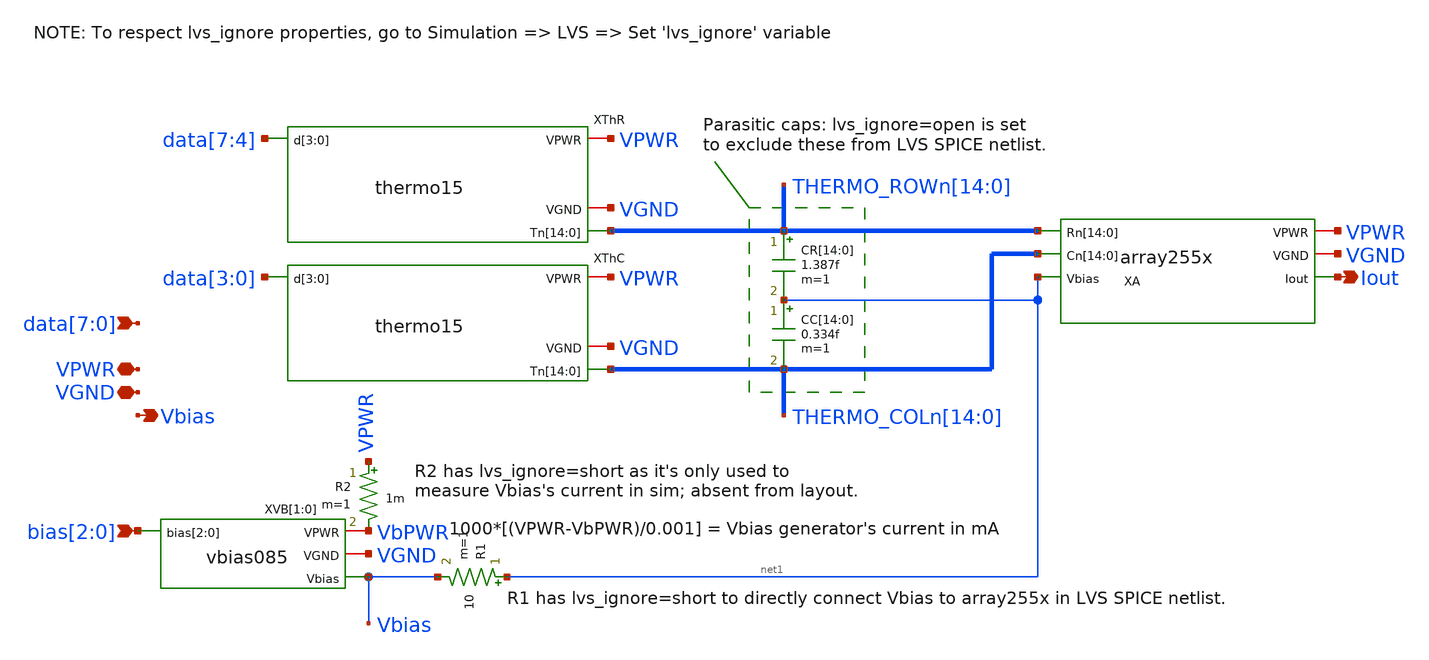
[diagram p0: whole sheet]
** sch_path: xschem/csdac255.sch
**.subckt csdac255 VPWR Iout VGND bias[2],bias[1],bias[0]
*+ data[7],data[6],data[5],data[4],data[3],data[2],data[1],data[0] Vbias
*.iopin VPWR
*.opin Iout
*.iopin VGND
*.ipin bias[2],bias[1],bias[0]
*.ipin data[7],data[6],data[5],data[4],data[3],data[2],data[1],data[0]
*.opin Vbias
XThR VPWR VGND THERMO_ROWn[14] THERMO_ROWn[13] THERMO_ROWn[12] THERMO_ROWn[11] THERMO_ROWn[10]
+ THERMO_ROWn[9] THERMO_ROWn[8] THERMO_ROWn[7] THERMO_ROWn[6] THERMO_ROWn[5] THERMO_ROWn[4] THERMO_ROWn[3]
+ THERMO_ROWn[2] THERMO_ROWn[1] THERMO_ROWn[0] data[7] data[6] data[5] data[4] thermo15
XA VPWR VGND THERMO_ROWn[14] THERMO_ROWn[13] THERMO_ROWn[12] THERMO_ROWn[11] THERMO_ROWn[10]
+ THERMO_ROWn[9] THERMO_ROWn[8] THERMO_ROWn[7] THERMO_ROWn[6] THERMO_ROWn[5] THERMO_ROWn[4] THERMO_ROWn[3]
+ THERMO_ROWn[2] THERMO_ROWn[1] THERMO_ROWn[0] THERMO_COLn[14] THERMO_COLn[13] THERMO_COLn[12] THERMO_COLn[11]
+ THERMO_COLn[10] THERMO_COLn[9] THERMO_COLn[8] THERMO_COLn[7] THERMO_COLn[6] THERMO_COLn[5] THERMO_COLn[4]
+ THERMO_COLn[3] THERMO_COLn[2] THERMO_COLn[1] THERMO_COLn[0] net1 Iout array255x
XThC VPWR VGND THERMO_COLn[14] THERMO_COLn[13] THERMO_COLn[12] THERMO_COLn[11] THERMO_COLn[10]
+ THERMO_COLn[9] THERMO_COLn[8] THERMO_COLn[7] THERMO_COLn[6] THERMO_COLn[5] THERMO_COLn[4] THERMO_COLn[3]
+ THERMO_COLn[2] THERMO_COLn[1] THERMO_COLn[0] data[3] data[2] data[1] data[0] thermo15
CR[14] THERMO_ROWn[14] net1 1.387f m=1
CR[13] THERMO_ROWn[13] net1 1.387f m=1
CR[12] THERMO_ROWn[12] net1 1.387f m=1
CR[11] THERMO_ROWn[11] net1 1.387f m=1
CR[10] THERMO_ROWn[10] net1 1.387f m=1
CR[9] THERMO_ROWn[9] net1 1.387f m=1
CR[8] THERMO_ROWn[8] net1 1.387f m=1
CR[7] THERMO_ROWn[7] net1 1.387f m=1
CR[6] THERMO_ROWn[6] net1 1.387f m=1
CR[5] THERMO_ROWn[5] net1 1.387f m=1
CR[4] THERMO_ROWn[4] net1 1.387f m=1
CR[3] THERMO_ROWn[3] net1 1.387f m=1
CR[2] THERMO_ROWn[2] net1 1.387f m=1
CR[1] THERMO_ROWn[1] net1 1.387f m=1
CR[0] THERMO_ROWn[0] net1 1.387f m=1
CC[14] net1 THERMO_COLn[14] 0.334f m=1
CC[13] net1 THERMO_COLn[13] 0.334f m=1
CC[12] net1 THERMO_COLn[12] 0.334f m=1
CC[11] net1 THERMO_COLn[11] 0.334f m=1
CC[10] net1 THERMO_COLn[10] 0.334f m=1
CC[9] net1 THERMO_COLn[9] 0.334f m=1
CC[8] net1 THERMO_COLn[8] 0.334f m=1
CC[7] net1 THERMO_COLn[7] 0.334f m=1
CC[6] net1 THERMO_COLn[6] 0.334f m=1
CC[5] net1 THERMO_COLn[5] 0.334f m=1
CC[4] net1 THERMO_COLn[4] 0.334f m=1
CC[3] net1 THERMO_COLn[3] 0.334f m=1
CC[2] net1 THERMO_COLn[2] 0.334f m=1
CC[1] net1 THERMO_COLn[1] 0.334f m=1
CC[0] net1 THERMO_COLn[0] 0.334f m=1
XVB[1] VbPWR VGND bias[2] bias[1] bias[0] Vbias vbias085
XVB[0] VbPWR VGND bias[2] bias[1] bias[0] Vbias vbias085
R1 net1 Vbias 10 m=1
R2 VPWR VbPWR 1m m=1
**.ends
.end
